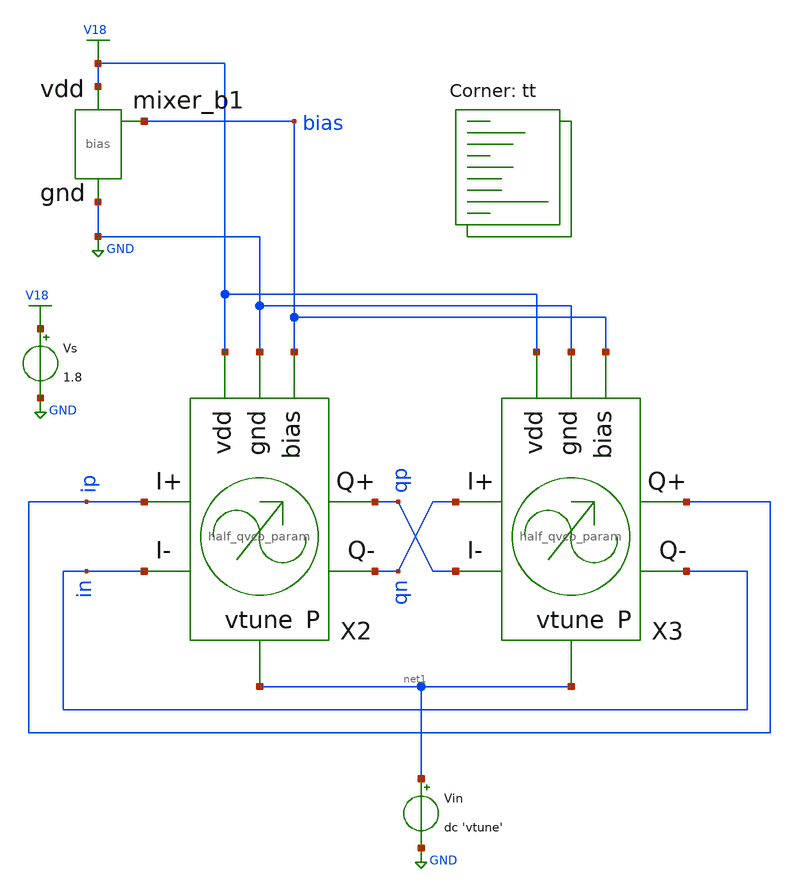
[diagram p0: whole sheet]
** sch_path: xschem/vco_transfer_tb.sch
**.subckt vco_transfer_tb
Vs V18 GND 1.8
Vin net1 GND dc 'vtune'
X1 bias V18 GND bias
X2 V18 GND bias ip in qp qn net1 half_qvco_param
X3 V18 GND bias qn qp ip in net1 half_qvco_param
**** begin user architecture code
.lib $::SKYWATER_MODELS/sky130.lib.spice tt


.param bias_width=10
.param bias_factor=10
.param m12_width=10
.param m12_fingers=2
.param m34_width=10
.param m34_fingers=2
.param capvar_width=30
.param capvar_length=30
.param capvar_mult=4
.param osc_ind=30n

.param vtune = 1





.subckt  sky130_fd_pr__ind_03_90 a b ct sub
R31 net27 b r='1e-2'
R26 a net23 r='1e-2'
C24 net35 net27 c='8.337e-15'
C25 net23 net37 c='53.8e-15'
C0 net27 net31 c='53.8e-15'
R1 sub net31 r='21.56'
R13 net23 net35 r='50.11'
R10 sub net37 r='21.56'
R0 net41 net27 r='1.019'
R9 net23 net39 r='1.019'
    L0 ct net41 l=760.5e-12
    L1 net39 ct l=760.5e-12
.ends sky130_fd_pr__ind_03_90

.subckt  sky130_fd_pr__ind_05_125 a b ct sub
R31 net27 b r='1e-2'
R26 a net23 r='1e-2'
C24 net35 net27 c='103.1e-15'
C25 net23 net37 c='357e-15'
C1 net27 net31 c='357e-15'
R3 sub net31 r='3.67e3'
R2 net41 net27 r='1.7645'
R13 net23 net35 r='9.312'
R10 sub net37 r='3.67e3'
R9 net23 net39 r='1.7645'
    L1 net39 ct l=2.895e-9
    L2 ct net41 l=2.895e-9
.ends sky130_fd_pr__ind_05_125


**** end user architecture code
**.ends

* expanding   symbol:  opensubghz/xschem/bias.sym # of pins=3
** sym_path: xschem/bias.sym
** sch_path: xschem/bias.sch
.subckt bias mixer_b1 vdd gnd
*.iopin vdd
*.opin mixer_b1
*.iopin gnd
XM1 net1 mixer_b1 gnd GND sky130_fd_pr__nfet_01v8 L=0.15 W=bias_width nf=1 ad='int((nf+1)/2) * W/nf * 0.29'
+ as='int((nf+2)/2) * W/nf * 0.29' pd='2*int((nf+1)/2) * (W/nf + 0.29)' ps='2*int((nf+2)/2) * (W/nf + 0.29)'
+ nrd='0.29 / W' nrs='0.29 / W' sa=0 sb=0 sd=0 mult=1 m=1
XR1 mixer_b1 vdd gnd sky130_fd_pr__res_xhigh_po_0p35 L=1.5 mult=1 m=1
Vsense mixer_b1 net1 0
.ends


* expanding   symbol:  opensubghz/xschem/half_qvco_param.sym # of pins=8
** sym_path: xschem/half_qvco_param.sym
** sch_path: xschem/half_qvco_param.sch
.subckt half_qvco_param vdd gnd bias I_p I_n Q_p Q_n vtune
*.iopin vdd
*.iopin gnd
*.ipin I_n
*.ipin bias
*.opin Q_p
*.opin Q_n
*.ipin I_p
*.ipin vtune
XM1 m4source Q_p net3 GND sky130_fd_pr__nfet_01v8 L=0.15 W='m12_width' nf='m12_fingers' ad='int((nf+1)/2) * W/nf * 0.29'
+ as='int((nf+2)/2) * W/nf * 0.29' pd='2*int((nf+1)/2) * (W/nf + 0.29)' ps='2*int((nf+2)/2) * (W/nf + 0.29)'
+ nrd='0.29 / W' nrs='0.29 / W' sa=0 sb=0 sd=0 mult=1 m=1
XM2 m3source Q_n net2 GND sky130_fd_pr__nfet_01v8 L=0.15 W='M12_width' nf='m12_fingers' ad='int((nf+1)/2) * W/nf * 0.29'
+ as='int((nf+2)/2) * W/nf * 0.29' pd='2*int((nf+1)/2) * (W/nf + 0.29)' ps='2*int((nf+2)/2) * (W/nf + 0.29)'
+ nrd='0.29 / W' nrs='0.29 / W' sa=0 sb=0 sd=0 mult=1 m=1
XC1 gnd Q_n vtune sky130_fd_pr__cap_var_lvt W='capvar_width' L='capvar_length' VM='capvar_mult' m='capvar_mult'
XC2 gnd Q_p vtune sky130_fd_pr__cap_var_lvt W='capvar_width' L='capvar_length' VM='capvar_mult' m='capvar_mult'
XM5 net1 bias gnd GND sky130_fd_pr__nfet_01v8 L=0.15 W='bias_width*bias_factor' nf='bias_factor' ad='int((nf+1)/2) * W/nf * 0.29'
+ as='int((nf+2)/2) * W/nf * 0.29' pd='2*int((nf+1)/2) * (W/nf + 0.29)' ps='2*int((nf+2)/2) * (W/nf + 0.29)'
+ nrd='0.29 / W' nrs='0.29 / W' sa=0 sb=0 sd=0 mult=1 m=1
XM3 Q_p I_n m3source GND sky130_fd_pr__nfet_01v8 L=0.15 W='m34_width' nf='m34_fingers' ad='int((nf+1)/2) * W/nf * 0.29'
+ as='int((nf+2)/2) * W/nf * 0.29' pd='2*int((nf+1)/2) * (W/nf + 0.29)' ps='2*int((nf+2)/2) * (W/nf + 0.29)'
+ nrd='0.29 / W' nrs='0.29 / W' sa=0 sb=0 sd=0 mult=1 m=1
XM4 Q_n I_p m4source GND sky130_fd_pr__nfet_01v8 L=0.15 W=m34_width nf=m34_fingers ad='int((nf+1)/2) * W/nf * 0.29'
+ as='int((nf+2)/2) * W/nf * 0.29' pd='2*int((nf+1)/2) * (W/nf + 0.29)' ps='2*int((nf+2)/2) * (W/nf + 0.29)'
+ nrd='0.29 / W' nrs='0.29 / W' sa=0 sb=0 sd=0 mult=1 m=1
Vsense1 cm0 net1 0
Vsense2a net2 cm0 0
Vsense2b net3 cm0 0
Vsense3b net5 Q_n 0
Vsense3a net4 Q_p 0
XL1 net5 net4 vdd gnd sky130_fd_pr__ind_03_90
.ends

.GLOBAL GND
.GLOBAL V18
.end
